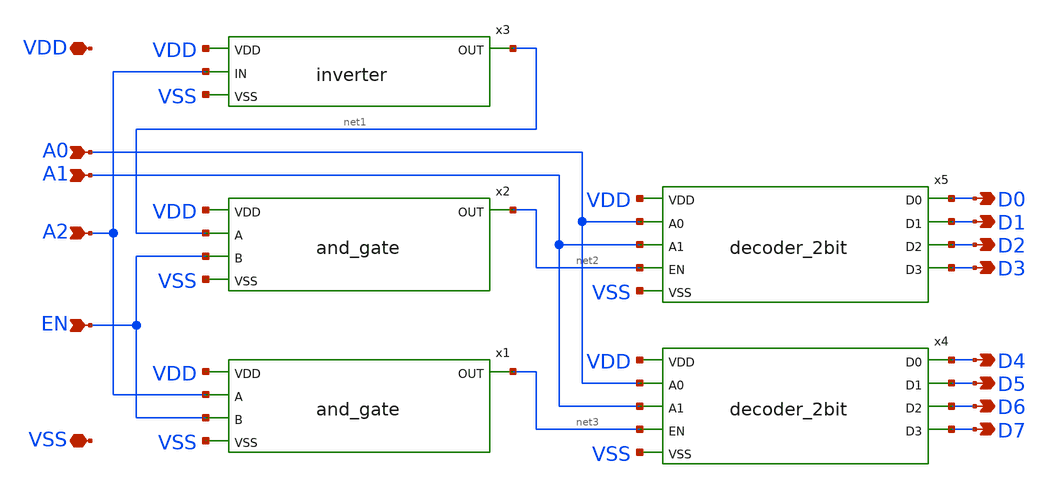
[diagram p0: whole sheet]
** sch_path: xschem/decoder_3bit.sch
**.subckt decoder_3bit VSS VDD A0 EN D0 D1 A1 D2 D3 A2 D4 D5 D6 D7
*.iopin VSS
*.iopin VDD
*.ipin A0
*.ipin EN
*.opin D0
*.opin D1
*.ipin A1
*.opin D2
*.opin D3
*.ipin A2
*.opin D4
*.opin D5
*.opin D6
*.opin D7
x1 VDD net3 A2 EN VSS and_gate
x2 VDD net2 net1 EN VSS and_gate
x3 VDD A2 net1 VSS inverter
x4 VDD A0 D4 D5 A1 net3 D6 D7 VSS decoder_2bit
x5 VDD A0 D0 D1 A1 net2 D2 D3 VSS decoder_2bit
**.ends
.end
